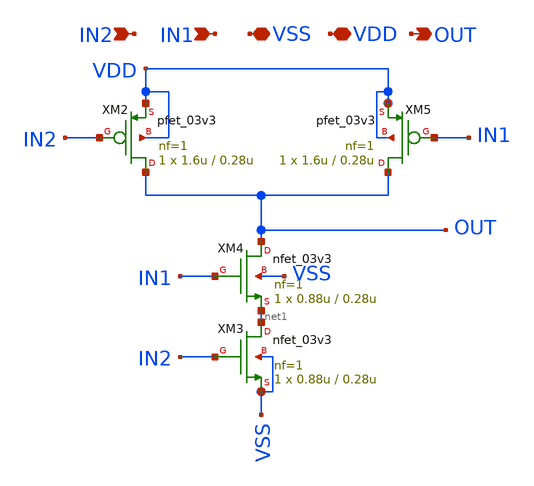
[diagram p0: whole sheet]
** sch_path: Clock_Generator_PAKISTAN_02/Schematics/NAND_dec_ibr.sch
**.subckt NAND_dec_ibr IN2 IN1 VSS VDD OUT
*.ipin IN2
*.ipin IN1
*.iopin VSS
*.iopin VDD
*.opin OUT
XM3 net1 IN2 VSS VSS nfet_03v3 L=0.28u W=0.88u nf=1 ad='int((nf+1)/2) * W/nf * 0.18u' as='int((nf+2)/2) * W/nf * 0.18u'
+ pd='2*int((nf+1)/2) * (W/nf + 0.18u)' ps='2*int((nf+2)/2) * (W/nf + 0.18u)' nrd='0.18u / W' nrs='0.18u / W'
+ sa=0 sb=0 sd=0 m=1
XM4 OUT IN1 net1 VSS nfet_03v3 L=0.28u W=0.88u nf=1 ad='int((nf+1)/2) * W/nf * 0.18u' as='int((nf+2)/2) * W/nf * 0.18u'
+ pd='2*int((nf+1)/2) * (W/nf + 0.18u)' ps='2*int((nf+2)/2) * (W/nf + 0.18u)' nrd='0.18u / W' nrs='0.18u / W'
+ sa=0 sb=0 sd=0 m=1
XM5 OUT IN1 VDD VDD pfet_03v3 L=0.28u W=1.6u nf=1 ad='int((nf+1)/2) * W/nf * 0.18u' as='int((nf+2)/2) * W/nf * 0.18u'
+ pd='2*int((nf+1)/2) * (W/nf + 0.18u)' ps='2*int((nf+2)/2) * (W/nf + 0.18u)' nrd='0.18u / W' nrs='0.18u / W'
+ sa=0 sb=0 sd=0 m=1
XM2 OUT IN2 VDD VDD pfet_03v3 L=0.28u W=1.6u nf=1 ad='int((nf+1)/2) * W/nf * 0.18u' as='int((nf+2)/2) * W/nf * 0.18u'
+ pd='2*int((nf+1)/2) * (W/nf + 0.18u)' ps='2*int((nf+2)/2) * (W/nf + 0.18u)' nrd='0.18u / W' nrs='0.18u / W'
+ sa=0 sb=0 sd=0 m=1
**.ends
.end
